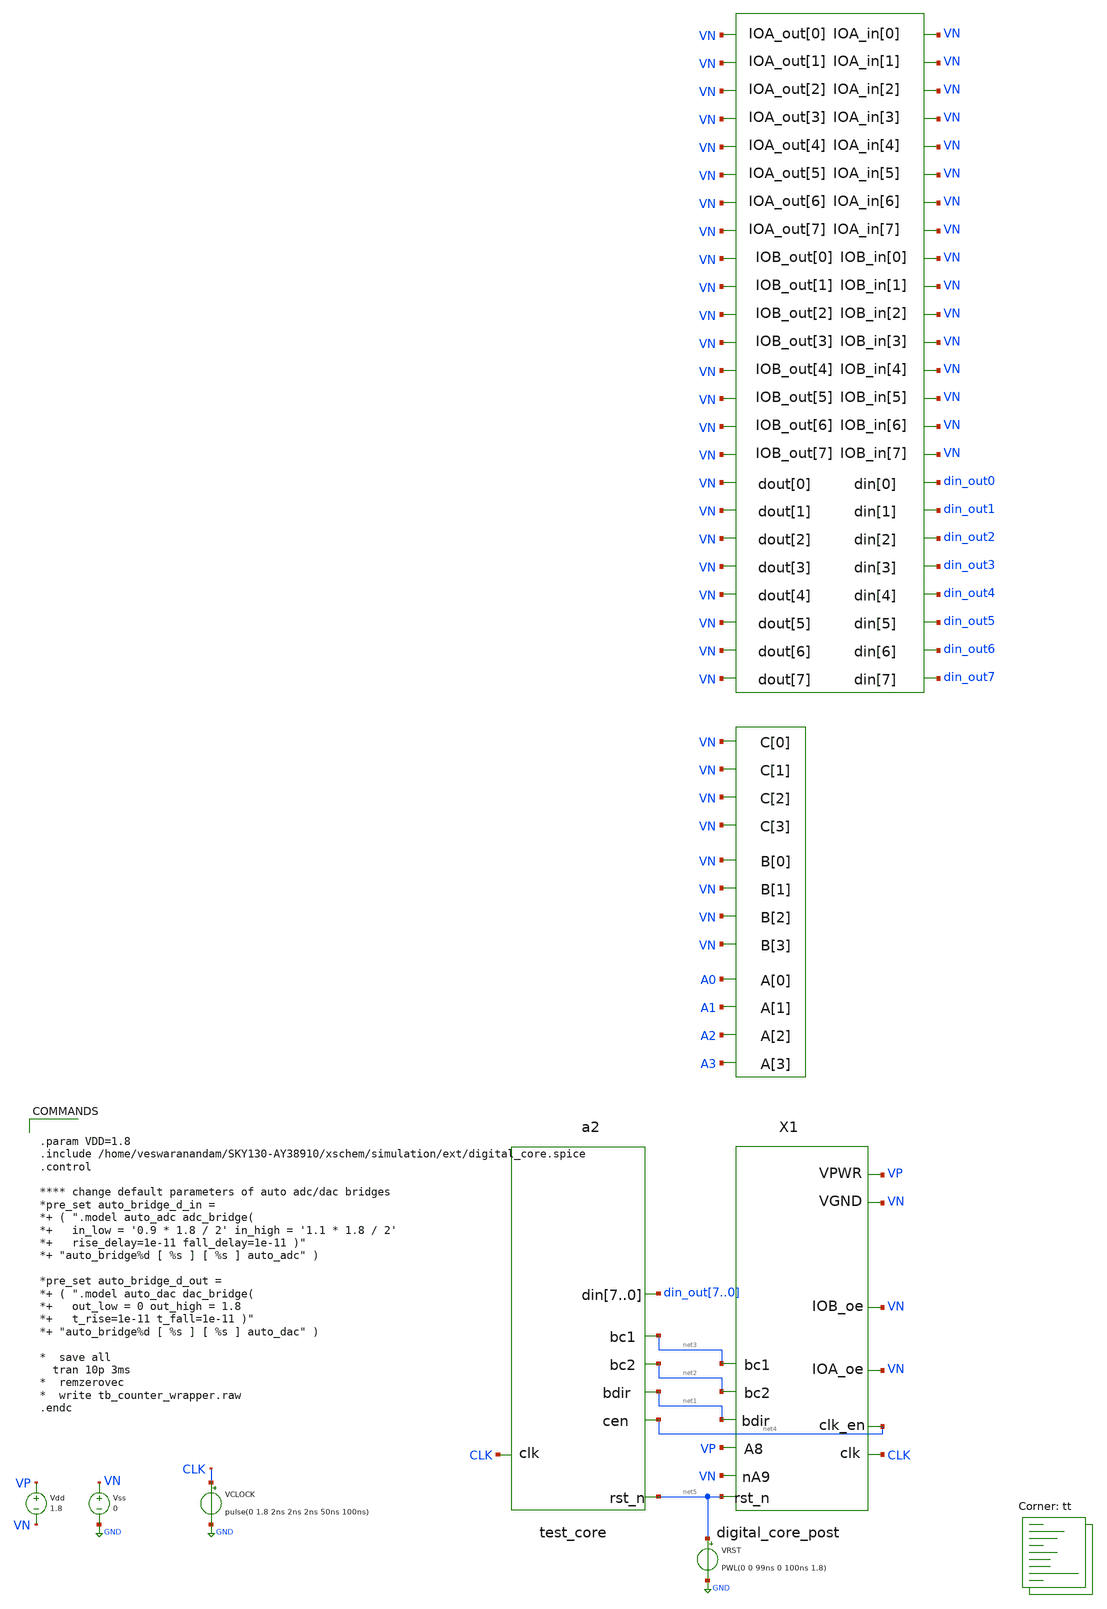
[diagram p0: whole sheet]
** sch_path: xschem/testbench_post.sch
**.subckt testbench_post
X1 VP A0 A1 A2 A3 VN VN VN VN VN VN VN VN VN VN VN VN VN VN VN VN VN VN VN VN VN VN VN VN VN VN VN
+ VN VN VN VN VN VN VN VN VN VN VN VN VN VN VN VN VP net3 net2 net1 CLK net4 din_out0 din_out1 din_out2
+ din_out3 din_out4 din_out5 din_out6 din_out7 VN VN VN VN VN VN VN VN VN net5 digital_core
a2 [ CLK net5 ] [ net4 net1 net3 net2 din_out7 din_out6 din_out5 din_out4 din_out3 din_out2 din_out1
+ din_out0 ] test_core
Vdd VP VN 1.8
Vss VN GND 0
VCLOCK CLK GND pulse(0 1.8 2ns 2ns 2ns 50ns 100ns)
VRST net5 GND PWL(0 0 99ns 0 100ns 1.8)
**** begin user architecture code


.param VDD=1.8
.include /home/veswaranandam/SKY130-AY38910/xschem/simulation/ext/digital_core.spice
.control

**** change default parameters of auto adc/dac bridges
*pre_set auto_bridge_d_in =
*+ ( ".model auto_adc adc_bridge(
*+   in_low = '0.9 * 1.8 / 2' in_high = '1.1 * 1.8 / 2'
*+   rise_delay=1e-11 fall_delay=1e-11 )"
*+ "auto_bridge%d [ %s ] [ %s ] auto_adc" )

*pre_set auto_bridge_d_out =
*+ ( ".model auto_dac dac_bridge(
*+   out_low = 0 out_high = 1.8
*+   t_rise=1e-11 t_fall=1e-11 )"
*+ "auto_bridge%d [ %s ] [ %s ] auto_dac" )

*  save all
  tran 10p 3ms
*  remzerovec
*  write tb_counter_wrapper.raw
.endc


.lib $::SKYWATER_MODELS/sky130.lib.spice tt
**** end user architecture code
**.ends
.GLOBAL GND
**** begin user architecture code
.model test_core d_cosim simulation="ivlng" sim_args=["test_core"] delay=1e-12
**** end user architecture code
.end
